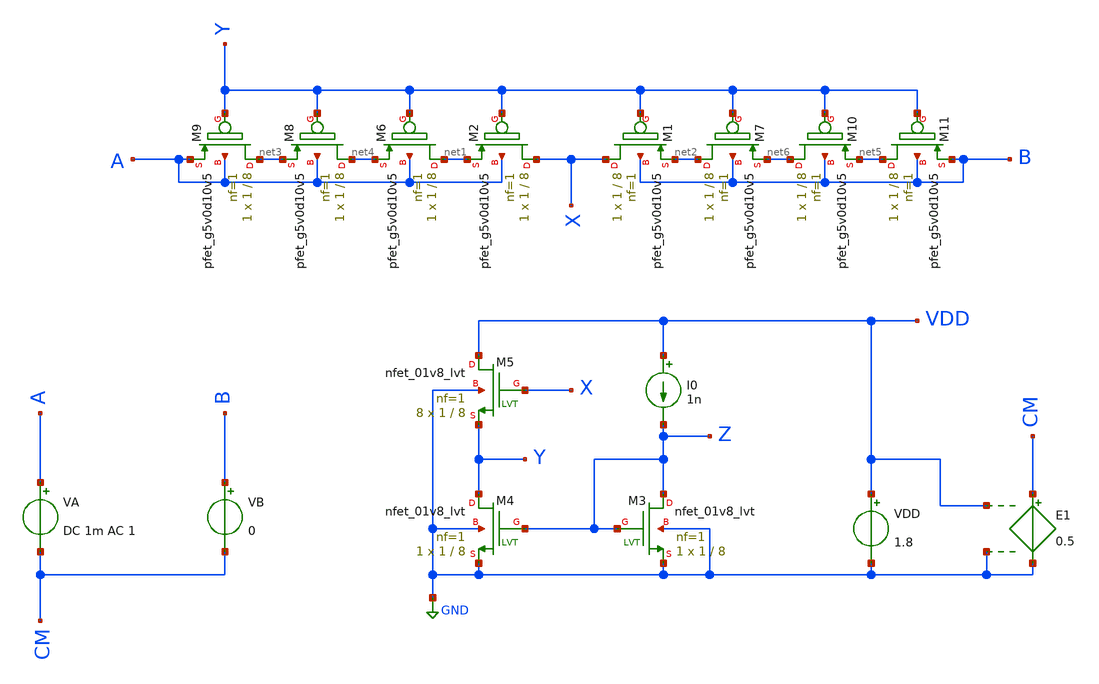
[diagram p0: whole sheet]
** sch_path: xschem/MISC/pseudo/pseudo_tune_tb2.sch
* Copyright 2020 Stefan Frederik Schippers
* Licensed under the Apache License, Version 2.0 (the "License");
* you may not use this file except in compliance with the License.
* You may obtain a copy of the License at
* https://www.apache.org/licenses/LICENSE-2.0
* Unless required by applicable law or agreed to in writing, software
* distributed under the License is distributed on an "AS IS" BASIS,
* WITHOUT WARRANTIES OR CONDITIONS OF ANY KIND, either express or implied.
* See the License for the specific language governing permissions and
* limitations under the License.
**.subckt pseudo_tune_tb2
XM1 X Y net2 B sky130_fd_pr__pfet_g5v0d10v5 L=8 W=1 nf=1 ad='int((nf+1)/2) * W/nf * 0.29' as='int((nf+2)/2) * W/nf * 0.29'
+ pd='2*int((nf+1)/2) * (W/nf + 0.29)' ps='2*int((nf+2)/2) * (W/nf + 0.29)' nrd='0.29 / W' nrs='0.29 / W'
+ sa=0 sb=0 sd=0 mult=1 m=1
XM2 X Y net1 A sky130_fd_pr__pfet_g5v0d10v5 L=8 W=1 nf=1 ad='int((nf+1)/2) * W/nf * 0.29' as='int((nf+2)/2) * W/nf * 0.29'
+ pd='2*int((nf+1)/2) * (W/nf + 0.29)' ps='2*int((nf+2)/2) * (W/nf + 0.29)' nrd='0.29 / W' nrs='0.29 / W'
+ sa=0 sb=0 sd=0 mult=1 m=1
VA A CM DC 1m AC 1
VB B CM 0
I0 VDD Z 1n
VDD VDD GND 1.8
E1 CM GND VDD GND 0.5
XM3 Z Z GND GND sky130_fd_pr__nfet_01v8_lvt L=8 W=1 nf=1 ad='int((nf+1)/2) * W/nf * 0.29' as='int((nf+2)/2) * W/nf * 0.29'
+ pd='2*int((nf+1)/2) * (W/nf + 0.29)' ps='2*int((nf+2)/2) * (W/nf + 0.29)' nrd='0.29 / W' nrs='0.29 / W'
+ sa=0 sb=0 sd=0 mult=1 m=1
XM4 Y Z GND GND sky130_fd_pr__nfet_01v8_lvt L=8 W=1 nf=1 ad='int((nf+1)/2) * W/nf * 0.29' as='int((nf+2)/2) * W/nf * 0.29'
+ pd='2*int((nf+1)/2) * (W/nf + 0.29)' ps='2*int((nf+2)/2) * (W/nf + 0.29)' nrd='0.29 / W' nrs='0.29 / W'
+ sa=0 sb=0 sd=0 mult=1 m=1
XM5 VDD X Y GND sky130_fd_pr__nfet_01v8_lvt L=8 W=1 nf=1 ad='int((nf+1)/2) * W/nf * 0.29' as='int((nf+2)/2) * W/nf * 0.29'
+ pd='2*int((nf+1)/2) * (W/nf + 0.29)' ps='2*int((nf+2)/2) * (W/nf + 0.29)' nrd='0.29 / W' nrs='0.29 / W'
+ sa=0 sb=0 sd=0 mult=8 m=8
XM6 net1 Y net4 A sky130_fd_pr__pfet_g5v0d10v5 L=8 W=1 nf=1 ad='int((nf+1)/2) * W/nf * 0.29' as='int((nf+2)/2) * W/nf * 0.29'
+ pd='2*int((nf+1)/2) * (W/nf + 0.29)' ps='2*int((nf+2)/2) * (W/nf + 0.29)' nrd='0.29 / W' nrs='0.29 / W'
+ sa=0 sb=0 sd=0 mult=1 m=1
XM7 net2 Y net6 B sky130_fd_pr__pfet_g5v0d10v5 L=8 W=1 nf=1 ad='int((nf+1)/2) * W/nf * 0.29' as='int((nf+2)/2) * W/nf * 0.29'
+ pd='2*int((nf+1)/2) * (W/nf + 0.29)' ps='2*int((nf+2)/2) * (W/nf + 0.29)' nrd='0.29 / W' nrs='0.29 / W'
+ sa=0 sb=0 sd=0 mult=1 m=1
XM8 net4 Y net3 A sky130_fd_pr__pfet_g5v0d10v5 L=8 W=1 nf=1 ad='int((nf+1)/2) * W/nf * 0.29' as='int((nf+2)/2) * W/nf * 0.29'
+ pd='2*int((nf+1)/2) * (W/nf + 0.29)' ps='2*int((nf+2)/2) * (W/nf + 0.29)' nrd='0.29 / W' nrs='0.29 / W'
+ sa=0 sb=0 sd=0 mult=1 m=1
XM9 net3 Y A A sky130_fd_pr__pfet_g5v0d10v5 L=8 W=1 nf=1 ad='int((nf+1)/2) * W/nf * 0.29' as='int((nf+2)/2) * W/nf * 0.29'
+ pd='2*int((nf+1)/2) * (W/nf + 0.29)' ps='2*int((nf+2)/2) * (W/nf + 0.29)' nrd='0.29 / W' nrs='0.29 / W'
+ sa=0 sb=0 sd=0 mult=1 m=1
XM10 net6 Y net5 B sky130_fd_pr__pfet_g5v0d10v5 L=8 W=1 nf=1 ad='int((nf+1)/2) * W/nf * 0.29' as='int((nf+2)/2) * W/nf * 0.29'
+ pd='2*int((nf+1)/2) * (W/nf + 0.29)' ps='2*int((nf+2)/2) * (W/nf + 0.29)' nrd='0.29 / W' nrs='0.29 / W'
+ sa=0 sb=0 sd=0 mult=1 m=1
XM11 net5 Y B B sky130_fd_pr__pfet_g5v0d10v5 L=8 W=1 nf=1 ad='int((nf+1)/2) * W/nf * 0.29' as='int((nf+2)/2) * W/nf * 0.29'
+ pd='2*int((nf+1)/2) * (W/nf + 0.29)' ps='2*int((nf+2)/2) * (W/nf + 0.29)' nrd='0.29 / W' nrs='0.29 / W'
+ sa=0 sb=0 sd=0 mult=1 m=1
**** begin user architecture code



.nodeset v(x) = 0.9
.param mc_mm_switch=0

.options gmin=1e-15
*.options rshunt = 1.0e15

.control
  op
  print x y z a b

  ac DEC 1 1 1
  print 1/abs(I(VA))

  dc VA -0.9 0.9 1.1m
  let r=abs(deriv(v(a))/deriv(i(va)))
  plot r ylog

.endc





.include /usr/share/pdk/sky130A/libs.ref/spi/sky130_fd_pr/sky130_fd_pr__pfet_g5v0d10v5__tt.corner.spice
.include /usr/share/pdk/sky130A/libs.ref/spi/sky130_fd_pr/sky130_fd_pr__pfet_g5v0d10v5__mismatch.corner.spice
.include /usr/share/pdk/sky130A/libs.ref/spi/sky130_fd_pr/sky130_fd_pr__nfet_g5v0d10v5__tt.corner.spice
.include /usr/share/pdk/sky130A/libs.ref/spi/sky130_fd_pr/sky130_fd_pr__nfet_g5v0d10v5__mismatch.corner.spice

.include /usr/share/pdk/sky130A/libs.ref/spi/sky130_fd_pr/sky130_fd_pr__nfet_01v8_lvt__tt.corner.spice
.include /usr/share/pdk/sky130A/libs.ref/spi/sky130_fd_pr/sky130_fd_pr__nfet_01v8_lvt__mismatch.corner.spice
.include /usr/share/pdk/sky130A/libs.ref/spi/sky130_fd_pr/sky130_fd_pr__pfet_01v8_lvt__tt.corner.spice
.include /usr/share/pdk/sky130A/libs.ref/spi/sky130_fd_pr/sky130_fd_pr__pfet_01v8_lvt__mismatch.corner.spice

*.include ~/OpenPDK/skywater-pdk/skywater-pdk/libraries/sky130_fd_pr/latest/models/all.spice
.include /usr/share/pdk/sky130A/libs.tech/ngspice/all.spice


**** end user architecture code
**.ends
.GLOBAL GND
.end
